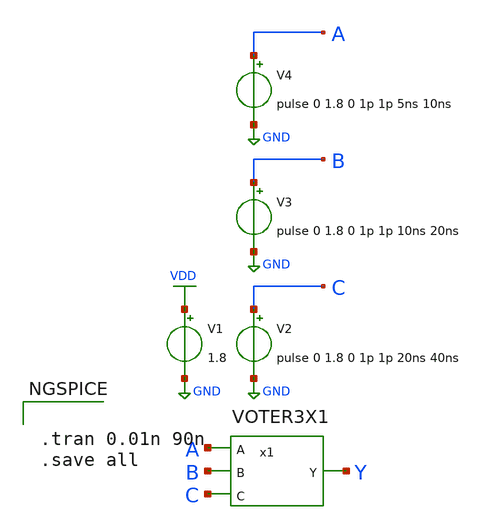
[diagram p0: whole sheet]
** sch_path: layout/xschem/sky130_rhbd/testbenches/test_VOTER3X1.sch
**.subckt test_VOTER3X1
V2 C GND pulse 0 1.8 0 1p 1p 20ns 40ns
V1 VDD GND 1.8
V3 B GND pulse 0 1.8 0 1p 1p 10ns 20ns
V4 A GND pulse 0 1.8 0 1p 1p 5ns 10ns
x1 Y A B C VDD GND VOTER3X1
**** begin user architecture code

.lib $::SKYWATER_MODELS/sky130.lib.spice tt


**** end user architecture code
**.ends
.GLOBAL VDD
.GLOBAL GND
**** begin user architecture code


.tran 0.01n 90n
.save all


**** end user architecture code
.end
